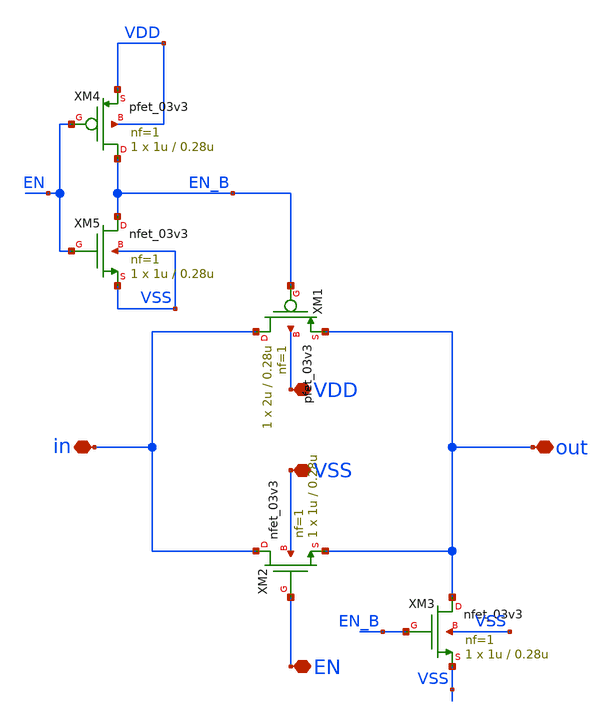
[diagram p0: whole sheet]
** sch_path: designs/digital/schematic/transmission_gate.sch
**.subckt transmission_gate VDD VSS in out EN
*.iopin VDD
*.iopin VSS
*.iopin in
*.iopin out
*.iopin EN
XM1 in EN_B out VDD pfet_03v3 L=0.28u W=2u nf=1 ad='int((nf+1)/2) * W/nf * 0.18u' as='int((nf+2)/2) * W/nf * 0.18u'
+ pd='2*int((nf+1)/2) * (W/nf + 0.18u)' ps='2*int((nf+2)/2) * (W/nf + 0.18u)' nrd='0.18u / W' nrs='0.18u / W'
+ sa=0 sb=0 sd=0 m=1
XM2 in EN out VSS nfet_03v3 L=0.28u W=1u nf=1 ad='int((nf+1)/2) * W/nf * 0.18u' as='int((nf+2)/2) * W/nf * 0.18u'
+ pd='2*int((nf+1)/2) * (W/nf + 0.18u)' ps='2*int((nf+2)/2) * (W/nf + 0.18u)' nrd='0.18u / W' nrs='0.18u / W'
+ sa=0 sb=0 sd=0 m=1
XM3 out EN_B VSS VSS nfet_03v3 L=0.28u W=1u nf=1 ad='int((nf+1)/2) * W/nf * 0.18u' as='int((nf+2)/2) * W/nf * 0.18u'
+ pd='2*int((nf+1)/2) * (W/nf + 0.18u)' ps='2*int((nf+2)/2) * (W/nf + 0.18u)' nrd='0.18u / W' nrs='0.18u / W'
+ sa=0 sb=0 sd=0 m=1
XM4 EN_B EN VDD VDD pfet_03v3 L=0.28u W=1u nf=1 ad='int((nf+1)/2) * W/nf * 0.18u' as='int((nf+2)/2) * W/nf * 0.18u'
+ pd='2*int((nf+1)/2) * (W/nf + 0.18u)' ps='2*int((nf+2)/2) * (W/nf + 0.18u)' nrd='0.18u / W' nrs='0.18u / W'
+ sa=0 sb=0 sd=0 m=1
XM5 EN_B EN VSS VSS nfet_03v3 L=0.28u W=1u nf=1 ad='int((nf+1)/2) * W/nf * 0.18u' as='int((nf+2)/2) * W/nf * 0.18u'
+ pd='2*int((nf+1)/2) * (W/nf + 0.18u)' ps='2*int((nf+2)/2) * (W/nf + 0.18u)' nrd='0.18u / W' nrs='0.18u / W'
+ sa=0 sb=0 sd=0 m=1
**.ends
.end
